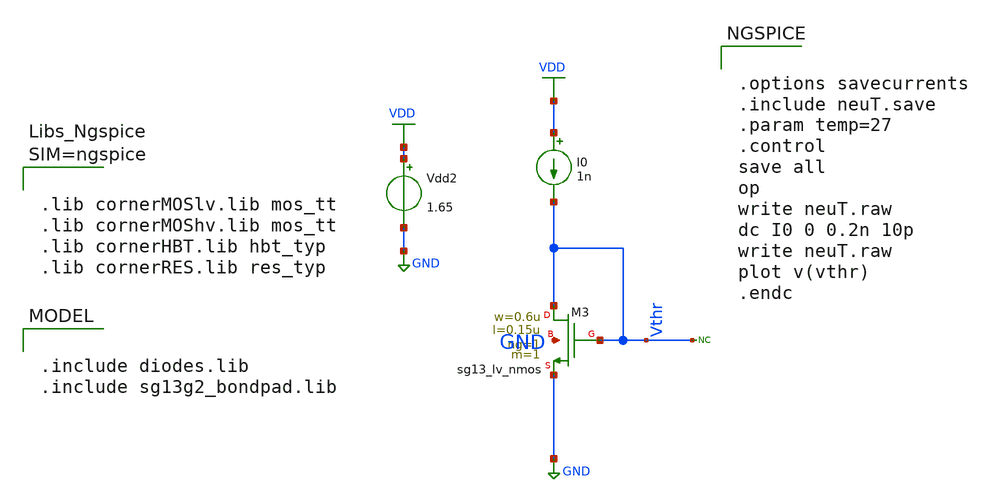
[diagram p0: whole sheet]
** sch_path: blocks/composite/dpi_adexp_neuron/design_data/xschem/dev/neuP.sch
**.subckt neuP
XM3 Vthr Vthr GND GND sg13_lv_nmos w=0.6u l=0.15u ng=1 m=1 mm_ok=1
Vdd2 VDD GND 1.65
* noconn Vthr
I0 VDD Vthr 1n
**** begin user architecture code

.include diodes.lib
.include sg13g2_bondpad.lib



.options savecurrents
.include neuT.save
.param temp=27
.control
save all
op
write neuT.raw
dc I0 0 0.2n 10p
write neuT.raw
plot v(vthr)
.endc





.lib cornerMOSlv.lib mos_tt
.lib cornerMOShv.lib mos_tt
.lib cornerHBT.lib hbt_typ
.lib cornerRES.lib res_typ



**** end user architecture code
**.ends
.GLOBAL GND
.GLOBAL VDD
.end
